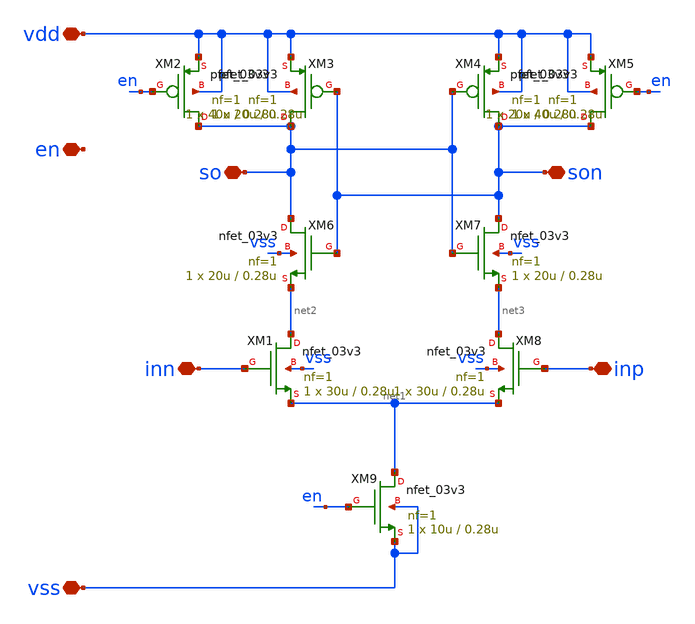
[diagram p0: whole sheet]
** sch_path: designs/libs/qw_core_analog_pkedit/StrongArmLatch.sch
**.subckt StrongArmLatch vdd vss en inn inp so son
*.iopin vdd
*.iopin vss
*.iopin en
*.iopin inn
*.iopin inp
*.iopin so
*.iopin son
XM1 net2 inn net1 vss nfet_03v3 L=0.28u W=30u nf=1 ad='int((nf+1)/2) * W/nf * 0.18u' as='int((nf+2)/2) * W/nf * 0.18u'
+ pd='2*int((nf+1)/2) * (W/nf + 0.18u)' ps='2*int((nf+2)/2) * (W/nf + 0.18u)' nrd='0.18u / W' nrs='0.18u / W'
+ sa=0 sb=0 sd=0 m=1
XM2 so en vdd vdd pfet_03v3 L=0.28u W=20u nf=1 ad='int((nf+1)/2) * W/nf * 0.18u' as='int((nf+2)/2) * W/nf * 0.18u'
+ pd='2*int((nf+1)/2) * (W/nf + 0.18u)' ps='2*int((nf+2)/2) * (W/nf + 0.18u)' nrd='0.18u / W' nrs='0.18u / W'
+ sa=0 sb=0 sd=0 m=1
XM3 so son vdd vdd pfet_03v3 L=0.28u W=40u nf=1 ad='int((nf+1)/2) * W/nf * 0.18u' as='int((nf+2)/2) * W/nf * 0.18u'
+ pd='2*int((nf+1)/2) * (W/nf + 0.18u)' ps='2*int((nf+2)/2) * (W/nf + 0.18u)' nrd='0.18u / W' nrs='0.18u / W'
+ sa=0 sb=0 sd=0 m=1
XM4 son so vdd vdd pfet_03v3 L=0.28u W=40u nf=1 ad='int((nf+1)/2) * W/nf * 0.18u' as='int((nf+2)/2) * W/nf * 0.18u'
+ pd='2*int((nf+1)/2) * (W/nf + 0.18u)' ps='2*int((nf+2)/2) * (W/nf + 0.18u)' nrd='0.18u / W' nrs='0.18u / W'
+ sa=0 sb=0 sd=0 m=1
XM5 son en vdd vdd pfet_03v3 L=0.28u W=20u nf=1 ad='int((nf+1)/2) * W/nf * 0.18u' as='int((nf+2)/2) * W/nf * 0.18u'
+ pd='2*int((nf+1)/2) * (W/nf + 0.18u)' ps='2*int((nf+2)/2) * (W/nf + 0.18u)' nrd='0.18u / W' nrs='0.18u / W'
+ sa=0 sb=0 sd=0 m=1
XM6 so son net2 vss nfet_03v3 L=0.28u W=20u nf=1 ad='int((nf+1)/2) * W/nf * 0.18u' as='int((nf+2)/2) * W/nf * 0.18u'
+ pd='2*int((nf+1)/2) * (W/nf + 0.18u)' ps='2*int((nf+2)/2) * (W/nf + 0.18u)' nrd='0.18u / W' nrs='0.18u / W'
+ sa=0 sb=0 sd=0 m=1
XM7 son so net3 vss nfet_03v3 L=0.28u W=20u nf=1 ad='int((nf+1)/2) * W/nf * 0.18u' as='int((nf+2)/2) * W/nf * 0.18u'
+ pd='2*int((nf+1)/2) * (W/nf + 0.18u)' ps='2*int((nf+2)/2) * (W/nf + 0.18u)' nrd='0.18u / W' nrs='0.18u / W'
+ sa=0 sb=0 sd=0 m=1
XM8 net3 inp net1 vss nfet_03v3 L=0.28u W=30u nf=1 ad='int((nf+1)/2) * W/nf * 0.18u' as='int((nf+2)/2) * W/nf * 0.18u'
+ pd='2*int((nf+1)/2) * (W/nf + 0.18u)' ps='2*int((nf+2)/2) * (W/nf + 0.18u)' nrd='0.18u / W' nrs='0.18u / W'
+ sa=0 sb=0 sd=0 m=1
XM9 net1 en vss vss nfet_03v3 L=0.28u W=10u nf=1 ad='int((nf+1)/2) * W/nf * 0.18u' as='int((nf+2)/2) * W/nf * 0.18u'
+ pd='2*int((nf+1)/2) * (W/nf + 0.18u)' ps='2*int((nf+2)/2) * (W/nf + 0.18u)' nrd='0.18u / W' nrs='0.18u / W'
+ sa=0 sb=0 sd=0 m=1
**.ends
.end
